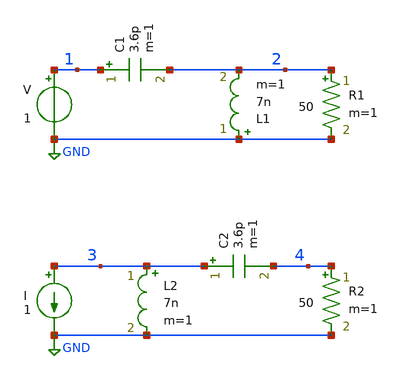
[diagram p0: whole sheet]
** sch_path: L-match.sch
**.subckt L-match
V 1 GND 1
C2 3 4 3.6p m=1
L2 3 GND 7n m=1
R2 4 GND 50 m=1
C1 1 2 3.6p m=1
L1 GND 2 7n m=1
R1 2 GND 50 m=1
I 3 GND 1
**** begin user architecture code



.option method=gear
.options savecurrents
.save all

.control
  tran 0.01ns 10ns
  alter @V[PULSE] [ 0 1 0 1ns ]
  alter @I[PULSE] [ 0 1 0 1ns ]

  ***
  alter @V[dc] 0
  alter @V[acmag] 1
  alter @I[dc] 0
  alter @I[acmag] 1
  ac lin 1001 100meg 10000meg

  ** impedance plot

.endc

**** end user architecture code
**.ends
.GLOBAL GND
.end
